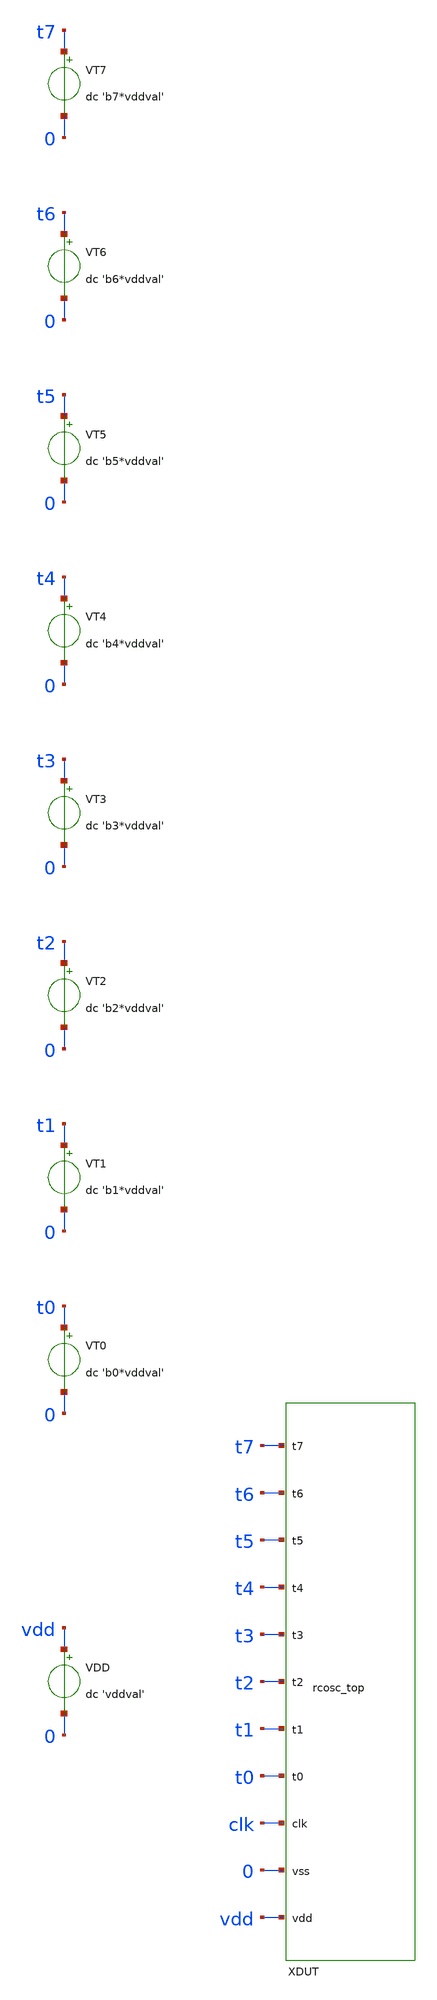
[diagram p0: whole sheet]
** sch_path: design/pvt_tb.sch
**.subckt pvt_tb
XXDUT vdd 0 clk t0 t1 t2 t3 t4 t5 t6 t7 rcosc_top
VDD vdd 0 dc 'vddval'
VT0 t0 0 dc 'b0*vddval'
VT1 t1 0 dc 'b1*vddval'
VT2 t2 0 dc 'b2*vddval'
VT3 t3 0 dc 'b3*vddval'
VT4 t4 0 dc 'b4*vddval'
VT5 t5 0 dc 'b5*vddval'
VT6 t6 0 dc 'b6*vddval'
VT7 t7 0 dc 'b7*vddval'
**** begin user architecture code


* --- per-run half of the deck (generated, NOT committed here) ---
*
* sim/pvt/pvt_sweep.py composes a self-contained run deck by substituting
* these two .include lines with generated content:
*
*   pvt_corner.spice   .include design.ngspice + the three .lib corner
*                      sections (fets / res / mimcap) for this run, the
*                      .temp line, and .param vddval / b0..b7
*   pvt_control.spice  the .control transient + rising-edge frequency
*                      measurement block for this run
*
* Keeping them out of the schematic is the same discipline smoke_test.sch
* uses for pdk_include.spice: no machine-specific absolute path and no
* run-specific corner state is baked into a committed .sch source.
.include pvt_corner.spice
.include pvt_control.spice


**** end user architecture code
**.ends

* expanding   symbol:  rcosc_top.sym # of pins=11
** sym_path: design/rcosc_top.sym
** sch_path: design/rcosc_top.sch
.subckt rcosc_top vdd vss clk t0 t1 t2 t3 t4 t5 t6 t7

*.iopin vdd
*.iopin vss
*.iopin clk
*.iopin t0
*.iopin t1
*.iopin t2
*.iopin t3
*.iopin t4
*.iopin t5
*.iopin t6
*.iopin t7
XXBIAS vdd vss vh vl ibias rcosc_bias
XXTRIM vdd vc vss t0 t1 t2 t3 t4 t5 t6 t7 vdd rcosc_trim_bank
XCTIMING vss vc cap_mim_1f0fF c_width=20u c_length=10u m=1
XXCMPH vdd vss ibias vc vh cmph_out rcosc_comparator
XXCMPL vdd vss ibias vl vc cmpl_out rcosc_comparator
XMDISCH vc clk vss vss nfet_03v3 L=0.5u W=20u nf=1 ad='int((nf+1)/2) * W/nf * 0.18u' as='int((nf+2)/2) * W/nf * 0.18u'
+ pd='2*int((nf+1)/2) * (W/nf + 0.18u)' ps='2*int((nf+2)/2) * (W/nf + 0.18u)' nrd='0.18u / W' nrs='0.18u / W'
+ sa=0 sb=0 sd=0 m=1
XMG1A qbar cmph_out vss vss nfet_03v3 L=0.5u W=2u nf=1 ad='int((nf+1)/2) * W/nf * 0.18u' as='int((nf+2)/2) * W/nf * 0.18u'
+ pd='2*int((nf+1)/2) * (W/nf + 0.18u)' ps='2*int((nf+2)/2) * (W/nf + 0.18u)' nrd='0.18u / W' nrs='0.18u / W'
+ sa=0 sb=0 sd=0 m=1
XMG1B qbar clk vss vss nfet_03v3 L=0.5u W=2u nf=1 ad='int((nf+1)/2) * W/nf * 0.18u' as='int((nf+2)/2) * W/nf * 0.18u'
+ pd='2*int((nf+1)/2) * (W/nf + 0.18u)' ps='2*int((nf+2)/2) * (W/nf + 0.18u)' nrd='0.18u / W' nrs='0.18u / W'
+ sa=0 sb=0 sd=0 m=1
XMG1C mid1 cmph_out vdd vdd pfet_03v3 L=0.5u W=4u nf=1 ad='int((nf+1)/2) * W/nf * 0.18u' as='int((nf+2)/2) * W/nf * 0.18u'
+ pd='2*int((nf+1)/2) * (W/nf + 0.18u)' ps='2*int((nf+2)/2) * (W/nf + 0.18u)' nrd='0.18u / W' nrs='0.18u / W'
+ sa=0 sb=0 sd=0 m=1
XMG1D qbar clk mid1 vdd pfet_03v3 L=0.5u W=4u nf=1 ad='int((nf+1)/2) * W/nf * 0.18u' as='int((nf+2)/2) * W/nf * 0.18u'
+ pd='2*int((nf+1)/2) * (W/nf + 0.18u)' ps='2*int((nf+2)/2) * (W/nf + 0.18u)' nrd='0.18u / W' nrs='0.18u / W'
+ sa=0 sb=0 sd=0 m=1
XMG2A clk cmpl_out vss vss nfet_03v3 L=0.5u W=2u nf=1 ad='int((nf+1)/2) * W/nf * 0.18u' as='int((nf+2)/2) * W/nf * 0.18u'
+ pd='2*int((nf+1)/2) * (W/nf + 0.18u)' ps='2*int((nf+2)/2) * (W/nf + 0.18u)' nrd='0.18u / W' nrs='0.18u / W'
+ sa=0 sb=0 sd=0 m=1
XMG2B clk qbar vss vss nfet_03v3 L=0.5u W=2u nf=1 ad='int((nf+1)/2) * W/nf * 0.18u' as='int((nf+2)/2) * W/nf * 0.18u'
+ pd='2*int((nf+1)/2) * (W/nf + 0.18u)' ps='2*int((nf+2)/2) * (W/nf + 0.18u)' nrd='0.18u / W' nrs='0.18u / W'
+ sa=0 sb=0 sd=0 m=1
XMG2C mid2 cmpl_out vdd vdd pfet_03v3 L=0.5u W=4u nf=1 ad='int((nf+1)/2) * W/nf * 0.18u' as='int((nf+2)/2) * W/nf * 0.18u'
+ pd='2*int((nf+1)/2) * (W/nf + 0.18u)' ps='2*int((nf+2)/2) * (W/nf + 0.18u)' nrd='0.18u / W' nrs='0.18u / W'
+ sa=0 sb=0 sd=0 m=1
XMG2D clk qbar mid2 vdd pfet_03v3 L=0.5u W=4u nf=1 ad='int((nf+1)/2) * W/nf * 0.18u' as='int((nf+2)/2) * W/nf * 0.18u'
+ pd='2*int((nf+1)/2) * (W/nf + 0.18u)' ps='2*int((nf+2)/2) * (W/nf + 0.18u)' nrd='0.18u / W' nrs='0.18u / W'
+ sa=0 sb=0 sd=0 m=1
.ends


* expanding   symbol:  rcosc_bias.sym # of pins=5
** sym_path: design/rcosc_bias.sym
** sch_path: design/rcosc_bias.sch
.subckt rcosc_bias vdd vss vh vl ibias

*.iopin vdd
*.iopin vss
*.iopin vh
*.iopin vl
*.iopin ibias
XRBA vdd vh vss ppolyf_u_1k r_width=2u r_length=100u m=1
XRBB vh vl vss ppolyf_u_1k r_width=2u r_length=100u m=1
XRBC vl vss vss ppolyf_u_1k r_width=2u r_length=100u m=1
XN1 ibias ibias vss vss nfet_03v3 L=1u W=2u nf=1 ad='int((nf+1)/2) * W/nf * 0.18u' as='int((nf+2)/2) * W/nf * 0.18u'
+ pd='2*int((nf+1)/2) * (W/nf + 0.18u)' ps='2*int((nf+2)/2) * (W/nf + 0.18u)' nrd='0.18u / W' nrs='0.18u / W'
+ sa=0 sb=0 sd=0 m=1
XN2 pb ibias n2s vss nfet_03v3 L=1u W=16u nf=8 ad='int((nf+1)/2) * W/nf * 0.18u' as='int((nf+2)/2) * W/nf * 0.18u'
+ pd='2*int((nf+1)/2) * (W/nf + 0.18u)' ps='2*int((nf+2)/2) * (W/nf + 0.18u)' nrd='0.18u / W' nrs='0.18u / W'
+ sa=0 sb=0 sd=0 m=1
XRZ n2s vss vss ppolyf_u_1k r_width=2u r_length=24u m=1
XP1 pb pb vdd vdd pfet_03v3 L=1u W=4u nf=1 ad='int((nf+1)/2) * W/nf * 0.18u' as='int((nf+2)/2) * W/nf * 0.18u'
+ pd='2*int((nf+1)/2) * (W/nf + 0.18u)' ps='2*int((nf+2)/2) * (W/nf + 0.18u)' nrd='0.18u / W' nrs='0.18u / W'
+ sa=0 sb=0 sd=0 m=1
XP2 ibias pb vdd vdd pfet_03v3 L=1u W=4u nf=1 ad='int((nf+1)/2) * W/nf * 0.18u' as='int((nf+2)/2) * W/nf * 0.18u'
+ pd='2*int((nf+1)/2) * (W/nf + 0.18u)' ps='2*int((nf+2)/2) * (W/nf + 0.18u)' nrd='0.18u / W' nrs='0.18u / W'
+ sa=0 sb=0 sd=0 m=1
XSEED vdd ibias vss ppolyf_u_1k r_width=2u r_length=4860u m=1
.ends


* expanding   symbol:  rcosc_trim_bank.sym # of pins=12
** sym_path: design/rcosc_trim_bank.sym
** sch_path: design/rcosc_trim_bank.sch
.subckt rcosc_trim_bank p m vss t0 t1 t2 t3 t4 t5 t6 t7 vdd

*.iopin p
*.iopin m
*.iopin vss
*.iopin t0
*.iopin t1
*.iopin t2
*.iopin t3
*.iopin t4
*.iopin t5
*.iopin t6
*.iopin t7
*.iopin vdd
XRFIX p c1 vss ppolyf_u_1k r_width=2u r_length=17.198u m=1
XR0 c1 c2 vss ppolyf_u_1k r_width=2u r_length=0.7482u m=1
XSW0 c1 t0 c2 vss nfet_03v3 L=0.28u W=24uu nf=1 ad='int((nf+1)/2) * W/nf * 0.18u' as='int((nf+2)/2) * W/nf * 0.18u'
+ pd='2*int((nf+1)/2) * (W/nf + 0.18u)' ps='2*int((nf+2)/2) * (W/nf + 0.18u)' nrd='0.18u / W' nrs='0.18u / W'
+ sa=0 sb=0 sd=0 m=1
XPW0 c2 tb0 c1 vdd pfet_03v3 L=0.28u W=24uu nf=1 ad='int((nf+1)/2) * W/nf * 0.18u' as='int((nf+2)/2) * W/nf * 0.18u'
+ pd='2*int((nf+1)/2) * (W/nf + 0.18u)' ps='2*int((nf+2)/2) * (W/nf + 0.18u)' nrd='0.18u / W' nrs='0.18u / W'
+ sa=0 sb=0 sd=0 m=1
XNINV0 tb0 t0 vss vss nfet_03v3 L=0.5u W=2u nf=1 ad='int((nf+1)/2) * W/nf * 0.18u' as='int((nf+2)/2) * W/nf * 0.18u'
+ pd='2*int((nf+1)/2) * (W/nf + 0.18u)' ps='2*int((nf+2)/2) * (W/nf + 0.18u)' nrd='0.18u / W' nrs='0.18u / W'
+ sa=0 sb=0 sd=0 m=1
XPINV0 tb0 t0 vdd vdd pfet_03v3 L=0.5u W=4u nf=1 ad='int((nf+1)/2) * W/nf * 0.18u' as='int((nf+2)/2) * W/nf * 0.18u'
+ pd='2*int((nf+1)/2) * (W/nf + 0.18u)' ps='2*int((nf+2)/2) * (W/nf + 0.18u)' nrd='0.18u / W' nrs='0.18u / W'
+ sa=0 sb=0 sd=0 m=1
XR1 c2 c3 vss ppolyf_u_1k r_width=2u r_length=1.4965u m=1
XSW1 c2 t1 c3 vss nfet_03v3 L=0.28u W=16uu nf=1 ad='int((nf+1)/2) * W/nf * 0.18u' as='int((nf+2)/2) * W/nf * 0.18u'
+ pd='2*int((nf+1)/2) * (W/nf + 0.18u)' ps='2*int((nf+2)/2) * (W/nf + 0.18u)' nrd='0.18u / W' nrs='0.18u / W'
+ sa=0 sb=0 sd=0 m=1
XPW1 c3 tb1 c2 vdd pfet_03v3 L=0.28u W=16uu nf=1 ad='int((nf+1)/2) * W/nf * 0.18u' as='int((nf+2)/2) * W/nf * 0.18u'
+ pd='2*int((nf+1)/2) * (W/nf + 0.18u)' ps='2*int((nf+2)/2) * (W/nf + 0.18u)' nrd='0.18u / W' nrs='0.18u / W'
+ sa=0 sb=0 sd=0 m=1
XNINV1 tb1 t1 vss vss nfet_03v3 L=0.5u W=2u nf=1 ad='int((nf+1)/2) * W/nf * 0.18u' as='int((nf+2)/2) * W/nf * 0.18u'
+ pd='2*int((nf+1)/2) * (W/nf + 0.18u)' ps='2*int((nf+2)/2) * (W/nf + 0.18u)' nrd='0.18u / W' nrs='0.18u / W'
+ sa=0 sb=0 sd=0 m=1
XPINV1 tb1 t1 vdd vdd pfet_03v3 L=0.5u W=4u nf=1 ad='int((nf+1)/2) * W/nf * 0.18u' as='int((nf+2)/2) * W/nf * 0.18u'
+ pd='2*int((nf+1)/2) * (W/nf + 0.18u)' ps='2*int((nf+2)/2) * (W/nf + 0.18u)' nrd='0.18u / W' nrs='0.18u / W'
+ sa=0 sb=0 sd=0 m=1
XR2 c3 c4 vss ppolyf_u_1k r_width=2u r_length=2.993u m=1
XSW2 c3 t2 c4 vss nfet_03v3 L=0.28u W=12uu nf=1 ad='int((nf+1)/2) * W/nf * 0.18u' as='int((nf+2)/2) * W/nf * 0.18u'
+ pd='2*int((nf+1)/2) * (W/nf + 0.18u)' ps='2*int((nf+2)/2) * (W/nf + 0.18u)' nrd='0.18u / W' nrs='0.18u / W'
+ sa=0 sb=0 sd=0 m=1
XPW2 c4 tb2 c3 vdd pfet_03v3 L=0.28u W=12uu nf=1 ad='int((nf+1)/2) * W/nf * 0.18u' as='int((nf+2)/2) * W/nf * 0.18u'
+ pd='2*int((nf+1)/2) * (W/nf + 0.18u)' ps='2*int((nf+2)/2) * (W/nf + 0.18u)' nrd='0.18u / W' nrs='0.18u / W'
+ sa=0 sb=0 sd=0 m=1
XNINV2 tb2 t2 vss vss nfet_03v3 L=0.5u W=2u nf=1 ad='int((nf+1)/2) * W/nf * 0.18u' as='int((nf+2)/2) * W/nf * 0.18u'
+ pd='2*int((nf+1)/2) * (W/nf + 0.18u)' ps='2*int((nf+2)/2) * (W/nf + 0.18u)' nrd='0.18u / W' nrs='0.18u / W'
+ sa=0 sb=0 sd=0 m=1
XPINV2 tb2 t2 vdd vdd pfet_03v3 L=0.5u W=4u nf=1 ad='int((nf+1)/2) * W/nf * 0.18u' as='int((nf+2)/2) * W/nf * 0.18u'
+ pd='2*int((nf+1)/2) * (W/nf + 0.18u)' ps='2*int((nf+2)/2) * (W/nf + 0.18u)' nrd='0.18u / W' nrs='0.18u / W'
+ sa=0 sb=0 sd=0 m=1
XR3 c4 c5 vss ppolyf_u_1k r_width=2u r_length=5.9859u m=1
XSW3 c4 t3 c5 vss nfet_03v3 L=0.28u W=8uu nf=1 ad='int((nf+1)/2) * W/nf * 0.18u' as='int((nf+2)/2) * W/nf * 0.18u'
+ pd='2*int((nf+1)/2) * (W/nf + 0.18u)' ps='2*int((nf+2)/2) * (W/nf + 0.18u)' nrd='0.18u / W' nrs='0.18u / W'
+ sa=0 sb=0 sd=0 m=1
XPW3 c5 tb3 c4 vdd pfet_03v3 L=0.28u W=8uu nf=1 ad='int((nf+1)/2) * W/nf * 0.18u' as='int((nf+2)/2) * W/nf * 0.18u'
+ pd='2*int((nf+1)/2) * (W/nf + 0.18u)' ps='2*int((nf+2)/2) * (W/nf + 0.18u)' nrd='0.18u / W' nrs='0.18u / W'
+ sa=0 sb=0 sd=0 m=1
XNINV3 tb3 t3 vss vss nfet_03v3 L=0.5u W=2u nf=1 ad='int((nf+1)/2) * W/nf * 0.18u' as='int((nf+2)/2) * W/nf * 0.18u'
+ pd='2*int((nf+1)/2) * (W/nf + 0.18u)' ps='2*int((nf+2)/2) * (W/nf + 0.18u)' nrd='0.18u / W' nrs='0.18u / W'
+ sa=0 sb=0 sd=0 m=1
XPINV3 tb3 t3 vdd vdd pfet_03v3 L=0.5u W=4u nf=1 ad='int((nf+1)/2) * W/nf * 0.18u' as='int((nf+2)/2) * W/nf * 0.18u'
+ pd='2*int((nf+1)/2) * (W/nf + 0.18u)' ps='2*int((nf+2)/2) * (W/nf + 0.18u)' nrd='0.18u / W' nrs='0.18u / W'
+ sa=0 sb=0 sd=0 m=1
XR4 c5 c6 vss ppolyf_u_1k r_width=2u r_length=11.9719u m=1
XSW4 c5 t4 c6 vss nfet_03v3 L=0.28u W=6uu nf=1 ad='int((nf+1)/2) * W/nf * 0.18u' as='int((nf+2)/2) * W/nf * 0.18u'
+ pd='2*int((nf+1)/2) * (W/nf + 0.18u)' ps='2*int((nf+2)/2) * (W/nf + 0.18u)' nrd='0.18u / W' nrs='0.18u / W'
+ sa=0 sb=0 sd=0 m=1
XPW4 c6 tb4 c5 vdd pfet_03v3 L=0.28u W=6uu nf=1 ad='int((nf+1)/2) * W/nf * 0.18u' as='int((nf+2)/2) * W/nf * 0.18u'
+ pd='2*int((nf+1)/2) * (W/nf + 0.18u)' ps='2*int((nf+2)/2) * (W/nf + 0.18u)' nrd='0.18u / W' nrs='0.18u / W'
+ sa=0 sb=0 sd=0 m=1
XNINV4 tb4 t4 vss vss nfet_03v3 L=0.5u W=2u nf=1 ad='int((nf+1)/2) * W/nf * 0.18u' as='int((nf+2)/2) * W/nf * 0.18u'
+ pd='2*int((nf+1)/2) * (W/nf + 0.18u)' ps='2*int((nf+2)/2) * (W/nf + 0.18u)' nrd='0.18u / W' nrs='0.18u / W'
+ sa=0 sb=0 sd=0 m=1
XPINV4 tb4 t4 vdd vdd pfet_03v3 L=0.5u W=4u nf=1 ad='int((nf+1)/2) * W/nf * 0.18u' as='int((nf+2)/2) * W/nf * 0.18u'
+ pd='2*int((nf+1)/2) * (W/nf + 0.18u)' ps='2*int((nf+2)/2) * (W/nf + 0.18u)' nrd='0.18u / W' nrs='0.18u / W'
+ sa=0 sb=0 sd=0 m=1
XR5 c6 c7 vss ppolyf_u_1k r_width=2u r_length=23.9438u m=1
XSW5 c6 t5 c7 vss nfet_03v3 L=0.28u W=5uu nf=1 ad='int((nf+1)/2) * W/nf * 0.18u' as='int((nf+2)/2) * W/nf * 0.18u'
+ pd='2*int((nf+1)/2) * (W/nf + 0.18u)' ps='2*int((nf+2)/2) * (W/nf + 0.18u)' nrd='0.18u / W' nrs='0.18u / W'
+ sa=0 sb=0 sd=0 m=1
XPW5 c7 tb5 c6 vdd pfet_03v3 L=0.28u W=5uu nf=1 ad='int((nf+1)/2) * W/nf * 0.18u' as='int((nf+2)/2) * W/nf * 0.18u'
+ pd='2*int((nf+1)/2) * (W/nf + 0.18u)' ps='2*int((nf+2)/2) * (W/nf + 0.18u)' nrd='0.18u / W' nrs='0.18u / W'
+ sa=0 sb=0 sd=0 m=1
XNINV5 tb5 t5 vss vss nfet_03v3 L=0.5u W=2u nf=1 ad='int((nf+1)/2) * W/nf * 0.18u' as='int((nf+2)/2) * W/nf * 0.18u'
+ pd='2*int((nf+1)/2) * (W/nf + 0.18u)' ps='2*int((nf+2)/2) * (W/nf + 0.18u)' nrd='0.18u / W' nrs='0.18u / W'
+ sa=0 sb=0 sd=0 m=1
XPINV5 tb5 t5 vdd vdd pfet_03v3 L=0.5u W=4u nf=1 ad='int((nf+1)/2) * W/nf * 0.18u' as='int((nf+2)/2) * W/nf * 0.18u'
+ pd='2*int((nf+1)/2) * (W/nf + 0.18u)' ps='2*int((nf+2)/2) * (W/nf + 0.18u)' nrd='0.18u / W' nrs='0.18u / W'
+ sa=0 sb=0 sd=0 m=1
XR6 c7 c8 vss ppolyf_u_1k r_width=2u r_length=47.8876u m=1
XSW6 c7 t6 c8 vss nfet_03v3 L=0.28u W=4uu nf=1 ad='int((nf+1)/2) * W/nf * 0.18u' as='int((nf+2)/2) * W/nf * 0.18u'
+ pd='2*int((nf+1)/2) * (W/nf + 0.18u)' ps='2*int((nf+2)/2) * (W/nf + 0.18u)' nrd='0.18u / W' nrs='0.18u / W'
+ sa=0 sb=0 sd=0 m=1
XPW6 c8 tb6 c7 vdd pfet_03v3 L=0.28u W=4uu nf=1 ad='int((nf+1)/2) * W/nf * 0.18u' as='int((nf+2)/2) * W/nf * 0.18u'
+ pd='2*int((nf+1)/2) * (W/nf + 0.18u)' ps='2*int((nf+2)/2) * (W/nf + 0.18u)' nrd='0.18u / W' nrs='0.18u / W'
+ sa=0 sb=0 sd=0 m=1
XNINV6 tb6 t6 vss vss nfet_03v3 L=0.5u W=2u nf=1 ad='int((nf+1)/2) * W/nf * 0.18u' as='int((nf+2)/2) * W/nf * 0.18u'
+ pd='2*int((nf+1)/2) * (W/nf + 0.18u)' ps='2*int((nf+2)/2) * (W/nf + 0.18u)' nrd='0.18u / W' nrs='0.18u / W'
+ sa=0 sb=0 sd=0 m=1
XPINV6 tb6 t6 vdd vdd pfet_03v3 L=0.5u W=4u nf=1 ad='int((nf+1)/2) * W/nf * 0.18u' as='int((nf+2)/2) * W/nf * 0.18u'
+ pd='2*int((nf+1)/2) * (W/nf + 0.18u)' ps='2*int((nf+2)/2) * (W/nf + 0.18u)' nrd='0.18u / W' nrs='0.18u / W'
+ sa=0 sb=0 sd=0 m=1
XR7 c8 m vss ppolyf_u_1k r_width=2u r_length=95.7751u m=1
XSW7 c8 t7 m vss nfet_03v3 L=0.28u W=3uu nf=1 ad='int((nf+1)/2) * W/nf * 0.18u' as='int((nf+2)/2) * W/nf * 0.18u'
+ pd='2*int((nf+1)/2) * (W/nf + 0.18u)' ps='2*int((nf+2)/2) * (W/nf + 0.18u)' nrd='0.18u / W' nrs='0.18u / W'
+ sa=0 sb=0 sd=0 m=1
XPW7 m tb7 c8 vdd pfet_03v3 L=0.28u W=3uu nf=1 ad='int((nf+1)/2) * W/nf * 0.18u' as='int((nf+2)/2) * W/nf * 0.18u'
+ pd='2*int((nf+1)/2) * (W/nf + 0.18u)' ps='2*int((nf+2)/2) * (W/nf + 0.18u)' nrd='0.18u / W' nrs='0.18u / W'
+ sa=0 sb=0 sd=0 m=1
XNINV7 tb7 t7 vss vss nfet_03v3 L=0.5u W=2u nf=1 ad='int((nf+1)/2) * W/nf * 0.18u' as='int((nf+2)/2) * W/nf * 0.18u'
+ pd='2*int((nf+1)/2) * (W/nf + 0.18u)' ps='2*int((nf+2)/2) * (W/nf + 0.18u)' nrd='0.18u / W' nrs='0.18u / W'
+ sa=0 sb=0 sd=0 m=1
XPINV7 tb7 t7 vdd vdd pfet_03v3 L=0.5u W=4u nf=1 ad='int((nf+1)/2) * W/nf * 0.18u' as='int((nf+2)/2) * W/nf * 0.18u'
+ pd='2*int((nf+1)/2) * (W/nf + 0.18u)' ps='2*int((nf+2)/2) * (W/nf + 0.18u)' nrd='0.18u / W' nrs='0.18u / W'
+ sa=0 sb=0 sd=0 m=1
.ends


* expanding   symbol:  rcosc_comparator.sym # of pins=6
** sym_path: design/rcosc_comparator.sym
** sch_path: design/rcosc_comparator.sch
.subckt rcosc_comparator vdd vss ibias inp inn out

*.iopin vdd
*.iopin vss
*.iopin ibias
*.iopin inp
*.iopin inn
*.iopin out
XMTAIL tail ibias vss vss nfet_03v3 L=1u W=16u nf=8 ad='int((nf+1)/2) * W/nf * 0.18u' as='int((nf+2)/2) * W/nf * 0.18u'
+ pd='2*int((nf+1)/2) * (W/nf + 0.18u)' ps='2*int((nf+2)/2) * (W/nf + 0.18u)' nrd='0.18u / W' nrs='0.18u / W'
+ sa=0 sb=0 sd=0 m=1
XMINP dp inp tail vss nfet_03v3 L=0.5u W=4u nf=1 ad='int((nf+1)/2) * W/nf * 0.18u' as='int((nf+2)/2) * W/nf * 0.18u'
+ pd='2*int((nf+1)/2) * (W/nf + 0.18u)' ps='2*int((nf+2)/2) * (W/nf + 0.18u)' nrd='0.18u / W' nrs='0.18u / W'
+ sa=0 sb=0 sd=0 m=1
XMINN dn inn tail vss nfet_03v3 L=0.5u W=4u nf=1 ad='int((nf+1)/2) * W/nf * 0.18u' as='int((nf+2)/2) * W/nf * 0.18u'
+ pd='2*int((nf+1)/2) * (W/nf + 0.18u)' ps='2*int((nf+2)/2) * (W/nf + 0.18u)' nrd='0.18u / W' nrs='0.18u / W'
+ sa=0 sb=0 sd=0 m=1
XMLOADA dn dn vdd vdd pfet_03v3 L=1u W=4u nf=1 ad='int((nf+1)/2) * W/nf * 0.18u' as='int((nf+2)/2) * W/nf * 0.18u'
+ pd='2*int((nf+1)/2) * (W/nf + 0.18u)' ps='2*int((nf+2)/2) * (W/nf + 0.18u)' nrd='0.18u / W' nrs='0.18u / W'
+ sa=0 sb=0 sd=0 m=1
XMLOADB dp dn vdd vdd pfet_03v3 L=1u W=4u nf=1 ad='int((nf+1)/2) * W/nf * 0.18u' as='int((nf+2)/2) * W/nf * 0.18u'
+ pd='2*int((nf+1)/2) * (W/nf + 0.18u)' ps='2*int((nf+2)/2) * (W/nf + 0.18u)' nrd='0.18u / W' nrs='0.18u / W'
+ sa=0 sb=0 sd=0 m=1
XMBUFP out dp vdd vdd pfet_03v3 L=0.5u W=4u nf=1 ad='int((nf+1)/2) * W/nf * 0.18u' as='int((nf+2)/2) * W/nf * 0.18u'
+ pd='2*int((nf+1)/2) * (W/nf + 0.18u)' ps='2*int((nf+2)/2) * (W/nf + 0.18u)' nrd='0.18u / W' nrs='0.18u / W'
+ sa=0 sb=0 sd=0 m=1
XMBUFN out dp vss vss nfet_03v3 L=0.5u W=1u nf=1 ad='int((nf+1)/2) * W/nf * 0.18u' as='int((nf+2)/2) * W/nf * 0.18u'
+ pd='2*int((nf+1)/2) * (W/nf + 0.18u)' ps='2*int((nf+2)/2) * (W/nf + 0.18u)' nrd='0.18u / W' nrs='0.18u / W'
+ sa=0 sb=0 sd=0 m=1
.ends

.end
